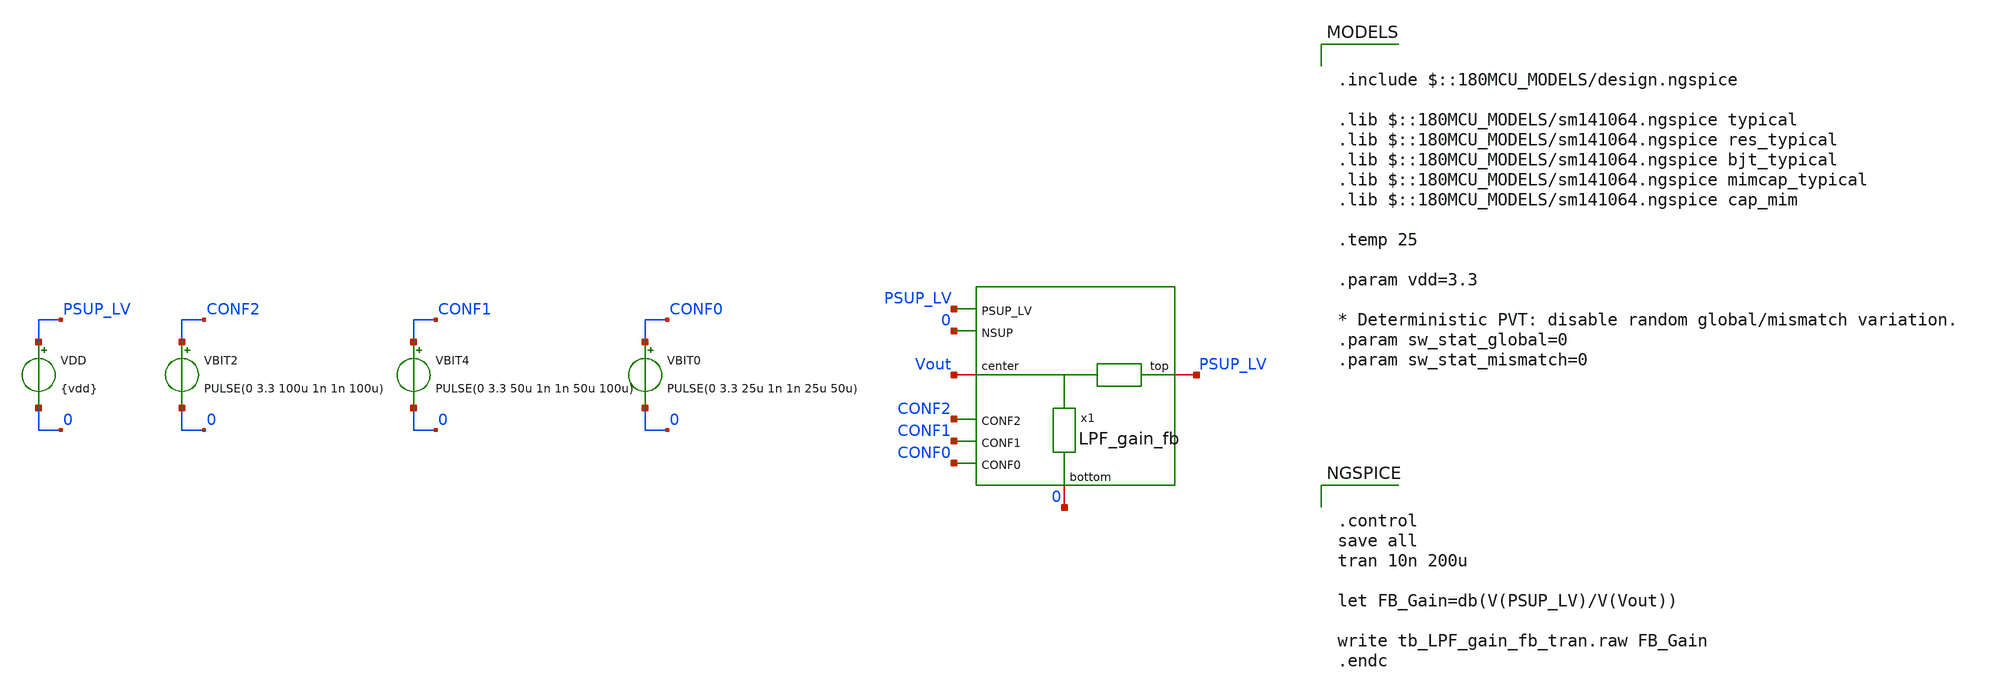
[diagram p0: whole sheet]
** sch_path: xschem/blocks/LPF_gain_fb/tb_LPF_gain_fb_tran.sch
**.subckt tb_LPF_gain_fb_tran
VBIT0 CONF0 0 PULSE(0 3.3 25u 1n 1n 25u 50u)
VBIT4 CONF1 0 PULSE(0 3.3 50u 1n 1n 50u 100u)
VDD PSUP_LV 0 {vdd}
VBIT2 CONF2 0 PULSE(0 3.3 100u 1n 1n 100u)
x1 PSUP_LV Vout PSUP_LV 0 CONF2 CONF1 CONF0 0 LPF_gain_fb
**** begin user architecture code

.include $::180MCU_MODELS/design.ngspice

.lib $::180MCU_MODELS/sm141064.ngspice typical
.lib $::180MCU_MODELS/sm141064.ngspice res_typical
.lib $::180MCU_MODELS/sm141064.ngspice bjt_typical
.lib $::180MCU_MODELS/sm141064.ngspice mimcap_typical
.lib $::180MCU_MODELS/sm141064.ngspice cap_mim

.temp 25

.param vdd=3.3

* Deterministic PVT: disable random global/mismatch variation.
.param sw_stat_global=0
.param sw_stat_mismatch=0



.control
save all
tran 10n 200u

let FB_Gain=db(V(PSUP_LV)/V(Vout))

write tb_LPF_gain_fb_tran.raw FB_Gain
.endc


**** end user architecture code
**.ends

* expanding   symbol:  blocks/LPF_gain_fb/LPF_gain_fb.sym # of pins=8
** sym_path: xschem/blocks/LPF_gain_fb/LPF_gain_fb.sym
** sch_path: xschem/blocks/LPF_gain_fb/LPF_gain_fb.sch
.subckt LPF_gain_fb top center PSUP_LV NSUP CONF2 CONF1 CONF0 bottom
*.iopin top
*.iopin center
*.iopin bottom
*.ipin PSUP_LV
*.ipin NSUP
*.ipin CONF1
*.ipin CONF2
*.ipin CONF0
XR1 net2 top PSUP_LV ppolyf_u_3k r_width=1e-6 r_length=625e-6 m=1
XR2 net1 net2 PSUP_LV ppolyf_u_3k r_width=1e-6 r_length=395e-6 m=1
XR3 center net4 PSUP_LV ppolyf_u_3k r_width=1e-6 r_length=111e-6 m=1
XR4 bottom net3 PSUP_LV ppolyf_u_3k r_width=1e-6 r_length=333e-6 m=1
x4 C0 net3 center nC0 net8 net9 transmission_gate
x1 C6 net2 top nC6 net10 net11 transmission_gate
x2 C5 net1 top nC5 net12 net13 transmission_gate
XR5 net4 net5 PSUP_LV ppolyf_u_3k r_width=1e-6 r_length=148e-6 m=1
XR6 net5 net6 PSUP_LV ppolyf_u_3k r_width=1e-6 r_length=198e-6 m=1
XR7 net6 net7 PSUP_LV ppolyf_u_3k r_width=1e-6 r_length=248e-6 m=1
XR8 net7 net1 PSUP_LV ppolyf_u_3k r_width=1e-6 r_length=352e-6 m=1
x5 C4 net7 top nC4 net14 net15 transmission_gate
x9 C3 net6 top nC3 net16 net17 transmission_gate
x10 C2 net5 top nC2 net18 net19 transmission_gate
x11 C1 net4 top nC1 net20 net21 transmission_gate
x12 nC0 center top C0 net22 net23 transmission_gate
x13 nC6 nCONF0 CONF2 PSUP_LV NSUP CONF1 nand_3
x14 nC5 CONF0 CONF2 PSUP_LV NSUP nCONF1 nand_3
x15 nC4 nCONF0 CONF2 PSUP_LV NSUP nCONF1 nand_3
x16 nC3 CONF0 nCONF2 PSUP_LV NSUP CONF1 nand_3
x17 nC2 nCONF0 nCONF2 PSUP_LV NSUP CONF1 nand_3
x18 nC1 CONF0 nCONF2 PSUP_LV NSUP nCONF1 nand_3
x19 C0 nCONF0 nCONF2 PSUP_LV NSUP nCONF1 nand_3
* noconn NSUP
* noconn PSUP_LV
x21 PSUP_LV nC6 C6 NSUP not
x22 PSUP_LV nC5 C5 NSUP not
* noconn NSUP
* noconn PSUP_LV
x26 PSUP_LV nC4 C4 NSUP not
x27 PSUP_LV nC3 C3 NSUP not
x28 PSUP_LV nC2 C2 NSUP not
x29 PSUP_LV nC1 C1 NSUP not
x30 PSUP_LV C0 nC0 NSUP not
* noconn NSUP
* noconn PSUP_LV
x3 PSUP_LV CONF0 nCONF0 NSUP not
x6 PSUP_LV CONF1 nCONF1 NSUP not
x7 PSUP_LV CONF2 nCONF2 NSUP not
.ends


* expanding   symbol:  blocks/transmission_gate/transmission_gate.sym # of pins=6
** sym_path: xschem/blocks/transmission_gate/transmission_gate.sym
** sch_path: xschem/blocks/transmission_gate/transmission_gate.sch
.subckt transmission_gate C A B nC VPOS VNEG
*.iopin A
*.iopin B
*.ipin C
*.ipin nC
*.ipin VPOS
*.ipin VNEG
XM3 A C B VNEG nfet_03v3 L=2u W=10u nf=1 ad='int((nf+1)/2) * W/nf * 0.18u' as='int((nf+2)/2) * W/nf * 0.18u'
+ pd='2*int((nf+1)/2) * (W/nf + 0.18u)' ps='2*int((nf+2)/2) * (W/nf + 0.18u)' nrd='0.18u / W' nrs='0.18u / W'
+ sa=0 sb=0 sd=0 m=2
XM4 A nC B VPOS pfet_03v3 L=2u W=10u nf=1 ad='int((nf+1)/2) * W/nf * 0.18u' as='int((nf+2)/2) * W/nf * 0.18u'
+ pd='2*int((nf+1)/2) * (W/nf + 0.18u)' ps='2*int((nf+2)/2) * (W/nf + 0.18u)' nrd='0.18u / W' nrs='0.18u / W'
+ sa=0 sb=0 sd=0 m=4
.ends


* expanding   symbol:  blocks/nand_3/nand_3.sym # of pins=8
** sym_path: xschem/blocks/nand_3/nand_3.sym
** sch_path: xschem/blocks/nand_3/nand_3.sch
.subckt nand_3 Y A C PSUP NSUP B
*.ipin PSUP
*.ipin NSUP
*.ipin A
*.ipin B
*.opin Y
*.ipin C
XM5 net1 C NSUP NSUP nfet_03v3 L=0.28u W=0.22u nf=1 ad='int((nf+1)/2) * W/nf * 0.18u' as='int((nf+2)/2) * W/nf * 0.18u'
+ pd='2*int((nf+1)/2) * (W/nf + 0.18u)' ps='2*int((nf+2)/2) * (W/nf + 0.18u)' nrd='0.18u / W' nrs='0.18u / W'
+ sa=0 sb=0 sd=0 m=1
XM1 Y A net2 NSUP nfet_03v3 L=0.28u W=0.22u nf=1 ad='int((nf+1)/2) * W/nf * 0.18u' as='int((nf+2)/2) * W/nf * 0.18u'
+ pd='2*int((nf+1)/2) * (W/nf + 0.18u)' ps='2*int((nf+2)/2) * (W/nf + 0.18u)' nrd='0.18u / W' nrs='0.18u / W'
+ sa=0 sb=0 sd=0 m=1
XM2 Y C PSUP PSUP pfet_03v3 L=0.28u W=0.5u nf=1 ad='int((nf+1)/2) * W/nf * 0.18u' as='int((nf+2)/2) * W/nf * 0.18u'
+ pd='2*int((nf+1)/2) * (W/nf + 0.18u)' ps='2*int((nf+2)/2) * (W/nf + 0.18u)' nrd='0.18u / W' nrs='0.18u / W'
+ sa=0 sb=0 sd=0 m=1
XM3 Y B PSUP PSUP pfet_03v3 L=0.28u W=0.5u nf=1 ad='int((nf+1)/2) * W/nf * 0.18u' as='int((nf+2)/2) * W/nf * 0.18u'
+ pd='2*int((nf+1)/2) * (W/nf + 0.18u)' ps='2*int((nf+2)/2) * (W/nf + 0.18u)' nrd='0.18u / W' nrs='0.18u / W'
+ sa=0 sb=0 sd=0 m=1
XM4 net2 B net1 NSUP nfet_03v3 L=0.28u W=0.22u nf=1 ad='int((nf+1)/2) * W/nf * 0.18u' as='int((nf+2)/2) * W/nf * 0.18u'
+ pd='2*int((nf+1)/2) * (W/nf + 0.18u)' ps='2*int((nf+2)/2) * (W/nf + 0.18u)' nrd='0.18u / W' nrs='0.18u / W'
+ sa=0 sb=0 sd=0 m=1
XM6 Y A PSUP PSUP pfet_03v3 L=0.28u W=0.5u nf=1 ad='int((nf+1)/2) * W/nf * 0.18u' as='int((nf+2)/2) * W/nf * 0.18u'
+ pd='2*int((nf+1)/2) * (W/nf + 0.18u)' ps='2*int((nf+2)/2) * (W/nf + 0.18u)' nrd='0.18u / W' nrs='0.18u / W'
+ sa=0 sb=0 sd=0 m=1
.ends


* expanding   symbol:  blocks/not/not.sym # of pins=6
** sym_path: xschem/blocks/not/not.sym
** sch_path: xschem/blocks/not/not.sch
.subckt not PSUP A B NSUP
*.ipin PSUP
*.ipin NSUP
*.ipin A
*.opin B
XM2 B A NSUP NSUP nfet_03v3 L=0.28u W=0.22u nf=1 ad='int((nf+1)/2) * W/nf * 0.18u' as='int((nf+2)/2) * W/nf * 0.18u'
+ pd='2*int((nf+1)/2) * (W/nf + 0.18u)' ps='2*int((nf+2)/2) * (W/nf + 0.18u)' nrd='0.18u / W' nrs='0.18u / W'
+ sa=0 sb=0 sd=0 m=1
XM1 B A PSUP PSUP pfet_03v3 L=0.28u W=0.5u nf=1 ad='int((nf+1)/2) * W/nf * 0.18u' as='int((nf+2)/2) * W/nf * 0.18u'
+ pd='2*int((nf+1)/2) * (W/nf + 0.18u)' ps='2*int((nf+2)/2) * (W/nf + 0.18u)' nrd='0.18u / W' nrs='0.18u / W'
+ sa=0 sb=0 sd=0 m=1
.ends

.end
